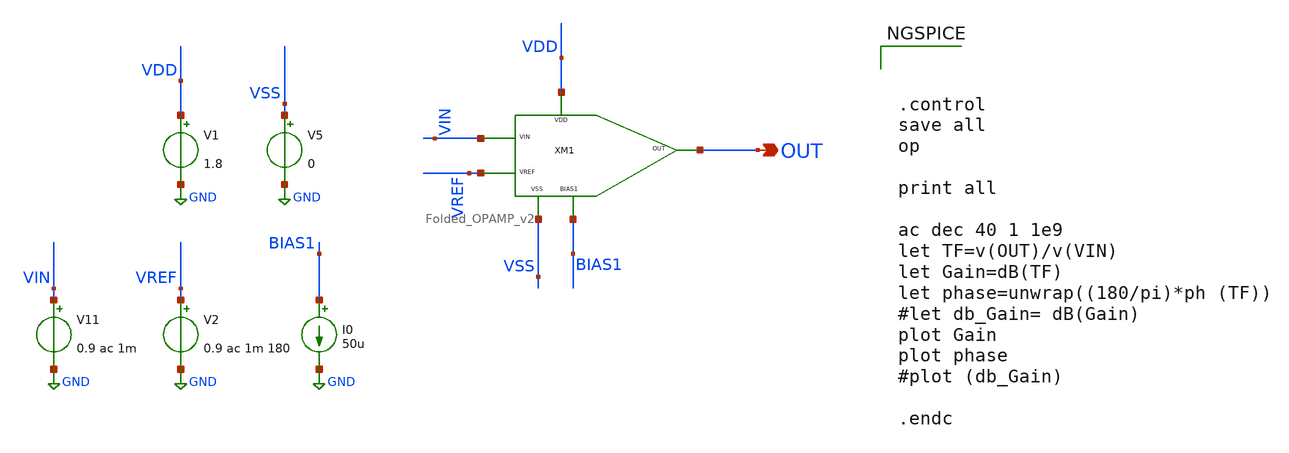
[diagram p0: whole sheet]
** sch_path: xschem/DC_DC_Converter_xschem/OTHERS/DC_DC_Converter_JV8/Folded_OPAMP/tb_Folded_OPAMP_v2.sch
**.subckt tb_Folded_OPAMP_v2 OUT
*.opin OUT
I0 BIAS1 GND 50u
V1 VDD GND 1.8
V5 VSS GND 0
V11 VIN GND 0.9 ac 1m
V2 VREF GND 0.9 ac 1m 180
XM1 VDD VSS BIAS1 OUT VIN VREF Folded_OPAMP_v2
**** begin user architecture code

** opencircuitdesign pdks install
.lib $::SKYWATER_MODELS/sky130.lib.spice tt





.control
save all
op

print all

ac dec 40 1 1e9
let TF=v(OUT)/v(VIN)
let Gain=dB(TF)
let phase=unwrap((180/pi)*ph (TF))
#let db_Gain= dB(Gain)
plot Gain
plot phase
#plot (db_Gain)

.endc


**** end user architecture code
**.ends

* expanding   symbol:  DC_DC_Converter/Folded_OPAMP/Folded_OPAMP_v2.sym # of pins=6
** sym_path: xschem/DC_DC_Converter_xschem/OTHERS/DC_DC_Converter_4/Folded_OPAMP/Folded_OPAMP_v2.sym
** sch_path: xschem/DC_DC_Converter_xschem/OTHERS/DC_DC_Converter_4/Folded_OPAMP/Folded_OPAMP_v2.sch
.subckt Folded_OPAMP_v2 VDD VSS BIAS1 OUT VIN VREF
*.iopin VSS
*.iopin VDD
*.opin OUT
*.ipin VIN
*.ipin VREF
*.iopin BIAS1
XM3 VOUTP BIAS1 VDD VDD sky130_fd_pr__pfet_01v8 L=0.9 W=3.91 nf=2 ad='int((nf+1)/2) * W/nf * 0.29' as='int((nf+2)/2) * W/nf * 0.29'
+ pd='2*int((nf+1)/2) * (W/nf + 0.29)' ps='2*int((nf+2)/2) * (W/nf + 0.29)' nrd='0.29 / W' nrs='0.29 / W'
+ sa=0 sb=0 sd=0 mult=5 m=5
XM4 VOUTN BIAS1 VDD VDD sky130_fd_pr__pfet_01v8 L=0.9 W=3.91 nf=2 ad='int((nf+1)/2) * W/nf * 0.29' as='int((nf+2)/2) * W/nf * 0.29'
+ pd='2*int((nf+1)/2) * (W/nf + 0.29)' ps='2*int((nf+2)/2) * (W/nf + 0.29)' nrd='0.29 / W' nrs='0.29 / W'
+ sa=0 sb=0 sd=0 mult=5 m=5
XM6 OUT BIAS2 VOUTN VDD sky130_fd_pr__pfet_01v8 L=0.9 W=3.91 nf=1 ad='int((nf+1)/2) * W/nf * 0.29' as='int((nf+2)/2) * W/nf * 0.29'
+ pd='2*int((nf+1)/2) * (W/nf + 0.29)' ps='2*int((nf+2)/2) * (W/nf + 0.29)' nrd='0.29 / W' nrs='0.29 / W'
+ sa=0 sb=0 sd=0 mult=5 m=5
XM7 net3 BIAS2 VOUTP VDD sky130_fd_pr__pfet_01v8 L=0.9 W=3.91 nf=1 ad='int((nf+1)/2) * W/nf * 0.29' as='int((nf+2)/2) * W/nf * 0.29'
+ pd='2*int((nf+1)/2) * (W/nf + 0.29)' ps='2*int((nf+2)/2) * (W/nf + 0.29)' nrd='0.29 / W' nrs='0.29 / W'
+ sa=0 sb=0 sd=0 mult=5 m=5
XM13 net4 net4 BIAS2 VSS sky130_fd_pr__nfet_01v8 L=0.9 W=5.14 nf=1 ad='int((nf+1)/2) * W/nf * 0.29' as='int((nf+2)/2) * W/nf * 0.29'
+ pd='2*int((nf+1)/2) * (W/nf + 0.29)' ps='2*int((nf+2)/2) * (W/nf + 0.29)' nrd='0.29 / W' nrs='0.29 / W'
+ sa=0 sb=0 sd=0 mult=1 m=1
XM14 BIAS3 BIAS3 net5 VSS sky130_fd_pr__nfet_01v8 L=0.9 W=7.714 nf=10 ad='int((nf+1)/2) * W/nf * 0.29'
+ as='int((nf+2)/2) * W/nf * 0.29' pd='2*int((nf+1)/2) * (W/nf + 0.29)' ps='2*int((nf+2)/2) * (W/nf + 0.29)'
+ nrd='0.29 / W' nrs='0.29 / W' sa=0 sb=0 sd=0 mult=1 m=1
XM15 BIAS2 BIAS2 VSS VSS sky130_fd_pr__nfet_01v8 L=0.9 W=5.14 nf=1 ad='int((nf+1)/2) * W/nf * 0.29' as='int((nf+2)/2) * W/nf * 0.29'
+ pd='2*int((nf+1)/2) * (W/nf + 0.29)' ps='2*int((nf+2)/2) * (W/nf + 0.29)' nrd='0.29 / W' nrs='0.29 / W'
+ sa=0 sb=0 sd=0 mult=1 m=1
XM17 VOUTP VIN net6 VSS sky130_fd_pr__nfet_01v8 L=0.9 W=3.91 nf=1 ad='int((nf+1)/2) * W/nf * 0.29' as='int((nf+2)/2) * W/nf * 0.29'
+ pd='2*int((nf+1)/2) * (W/nf + 0.29)' ps='2*int((nf+2)/2) * (W/nf + 0.29)' nrd='0.29 / W' nrs='0.29 / W'
+ sa=0 sb=0 sd=0 mult=10 m=10
XM18 VOUTN VREF net6 VSS sky130_fd_pr__nfet_01v8 L=0.9 W=3.91 nf=1 ad='int((nf+1)/2) * W/nf * 0.29' as='int((nf+2)/2) * W/nf * 0.29'
+ pd='2*int((nf+1)/2) * (W/nf + 0.29)' ps='2*int((nf+2)/2) * (W/nf + 0.29)' nrd='0.29 / W' nrs='0.29 / W'
+ sa=0 sb=0 sd=0 mult=10 m=10
XM10 OUT BIAS3 net1 VSS sky130_fd_pr__nfet_01v8 L=0.9 W=3.91 nf=1 ad='int((nf+1)/2) * W/nf * 0.29' as='int((nf+2)/2) * W/nf * 0.29'
+ pd='2*int((nf+1)/2) * (W/nf + 0.29)' ps='2*int((nf+2)/2) * (W/nf + 0.29)' nrd='0.29 / W' nrs='0.29 / W'
+ sa=0 sb=0 sd=0 mult=5 m=5
XM12 net3 BIAS3 net2 VSS sky130_fd_pr__nfet_01v8 L=0.9 W=3.91 nf=1 ad='int((nf+1)/2) * W/nf * 0.29' as='int((nf+2)/2) * W/nf * 0.29'
+ pd='2*int((nf+1)/2) * (W/nf + 0.29)' ps='2*int((nf+2)/2) * (W/nf + 0.29)' nrd='0.29 / W' nrs='0.29 / W'
+ sa=0 sb=0 sd=0 mult=5 m=5
XM8 net5 net5 VSS VSS sky130_fd_pr__nfet_01v8 L=0.9 W=7.714 nf=1 ad='int((nf+1)/2) * W/nf * 0.29' as='int((nf+2)/2) * W/nf * 0.29'
+ pd='2*int((nf+1)/2) * (W/nf + 0.29)' ps='2*int((nf+2)/2) * (W/nf + 0.29)' nrd='0.29 / W' nrs='0.29 / W'
+ sa=0 sb=0 sd=0 mult=1 m=1
XM9 net6 net5 VSS VSS sky130_fd_pr__nfet_01v8 L=0.9 W=7.82 nf=1 ad='int((nf+1)/2) * W/nf * 0.29' as='int((nf+2)/2) * W/nf * 0.29'
+ pd='2*int((nf+1)/2) * (W/nf + 0.29)' ps='2*int((nf+2)/2) * (W/nf + 0.29)' nrd='0.29 / W' nrs='0.29 / W'
+ sa=0 sb=0 sd=0 mult=10 m=10
XM5 net2 net3 VSS VSS sky130_fd_pr__nfet_01v8 L=0.9 W=3.91 nf=1 ad='int((nf+1)/2) * W/nf * 0.29' as='int((nf+2)/2) * W/nf * 0.29'
+ pd='2*int((nf+1)/2) * (W/nf + 0.29)' ps='2*int((nf+2)/2) * (W/nf + 0.29)' nrd='0.29 / W' nrs='0.29 / W'
+ sa=0 sb=0 sd=0 mult=5 m=5
XM11 net1 net3 VSS VSS sky130_fd_pr__nfet_01v8 L=0.9 W=3.91 nf=1 ad='int((nf+1)/2) * W/nf * 0.29' as='int((nf+2)/2) * W/nf * 0.29'
+ pd='2*int((nf+1)/2) * (W/nf + 0.29)' ps='2*int((nf+2)/2) * (W/nf + 0.29)' nrd='0.29 / W' nrs='0.29 / W'
+ sa=0 sb=0 sd=0 mult=5 m=5
XM1 BIAS1 BIAS1 VDD VDD sky130_fd_pr__pfet_01v8 L=0.9 W=7.714 nf=1 ad='int((nf+1)/2) * W/nf * 0.29' as='int((nf+2)/2) * W/nf * 0.29'
+ pd='2*int((nf+1)/2) * (W/nf + 0.29)' ps='2*int((nf+2)/2) * (W/nf + 0.29)' nrd='0.29 / W' nrs='0.29 / W'
+ sa=0 sb=0 sd=0 mult=1 m=1
XM2 BIAS3 BIAS1 VDD VDD sky130_fd_pr__pfet_01v8 L=0.9 W=7.714 nf=1 ad='int((nf+1)/2) * W/nf * 0.29' as='int((nf+2)/2) * W/nf * 0.29'
+ pd='2*int((nf+1)/2) * (W/nf + 0.29)' ps='2*int((nf+2)/2) * (W/nf + 0.29)' nrd='0.29 / W' nrs='0.29 / W'
+ sa=0 sb=0 sd=0 mult=1 m=1
XR1 net4 VDD VSS sky130_fd_pr__res_high_po_0p35 L=1 mult=1 m=1
XR2 VSS net4 VSS sky130_fd_pr__res_high_po_0p35 L=1 mult=1 m=1
.ends

.GLOBAL GND
.end
